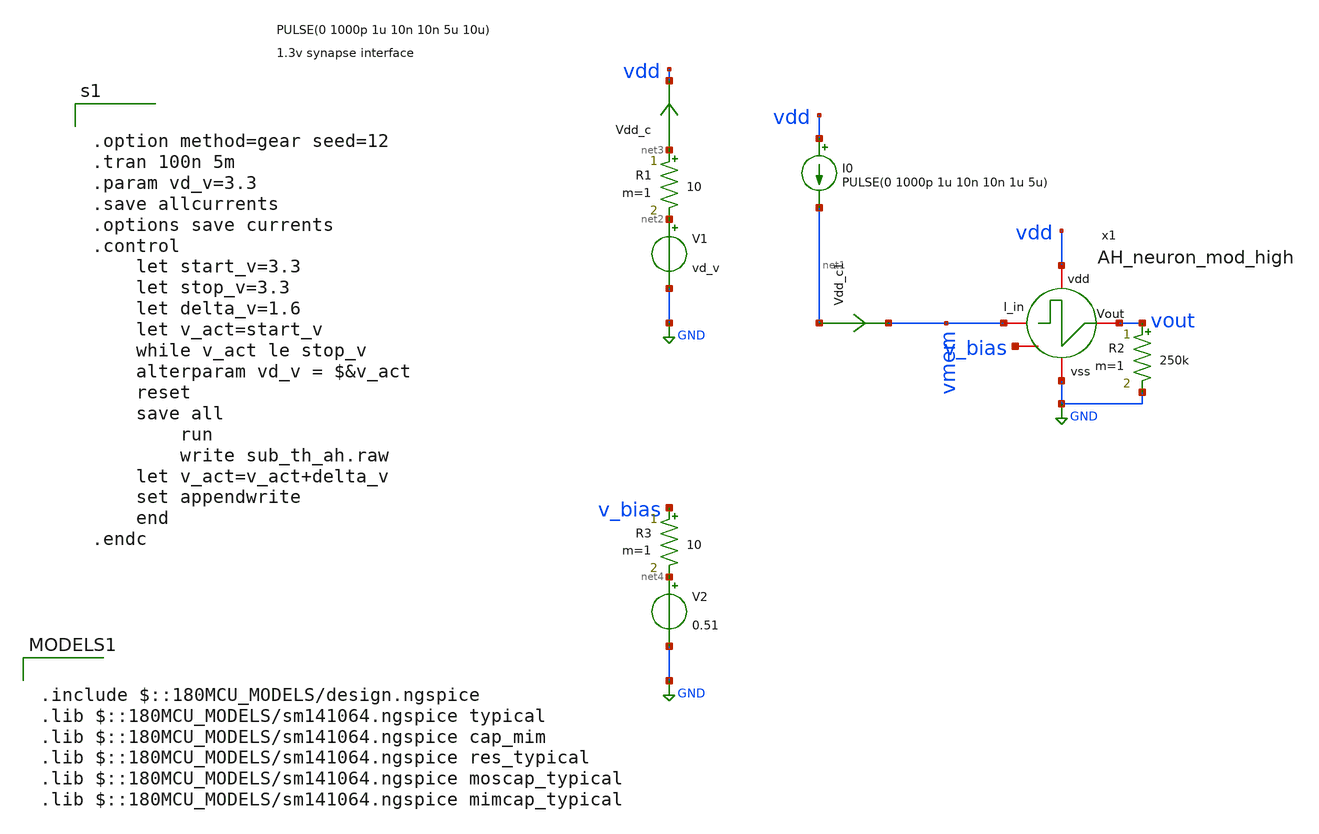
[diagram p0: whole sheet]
** sch_path: designs/libs/tb_AH_neuron/AH_neuron_mod.sch
**.subckt AH_neuron_mod
V1 net2 GND vd_v
Vdd_c net3 vdd 0
.save i(vdd_c)
I0 vdd net1 PULSE(0 1000p 1u 10n 10n 1u 5u)
R1 net3 net2 10 m=1
R2 vout GND 250k m=1
Vdd_c1 net1 vmem 0
.save i(vdd_c1)
x1 vdd vmem vout GND v_bias AH_neuron_mod_high
V2 net4 GND 0.51
R3 v_bias net4 10 m=1
**** begin user architecture code


.option method=gear seed=12
.tran 100n 5m
.param vd_v=3.3
.save allcurrents
.options save currents
.control
    let start_v=3.3
    let stop_v=3.3
    let delta_v=1.6
    let v_act=start_v
    while v_act le stop_v
	alterparam vd_v = $&v_act
	reset
	save all
        run
        write sub_th_ah.raw
	let v_act=v_act+delta_v
	set appendwrite
    end
.endc



.include $::180MCU_MODELS/design.ngspice
.lib $::180MCU_MODELS/sm141064.ngspice typical
.lib $::180MCU_MODELS/sm141064.ngspice cap_mim
.lib $::180MCU_MODELS/sm141064.ngspice res_typical
.lib $::180MCU_MODELS/sm141064.ngspice moscap_typical
.lib $::180MCU_MODELS/sm141064.ngspice mimcap_typical

**** end user architecture code
**.ends
.GLOBAL GND
.end
